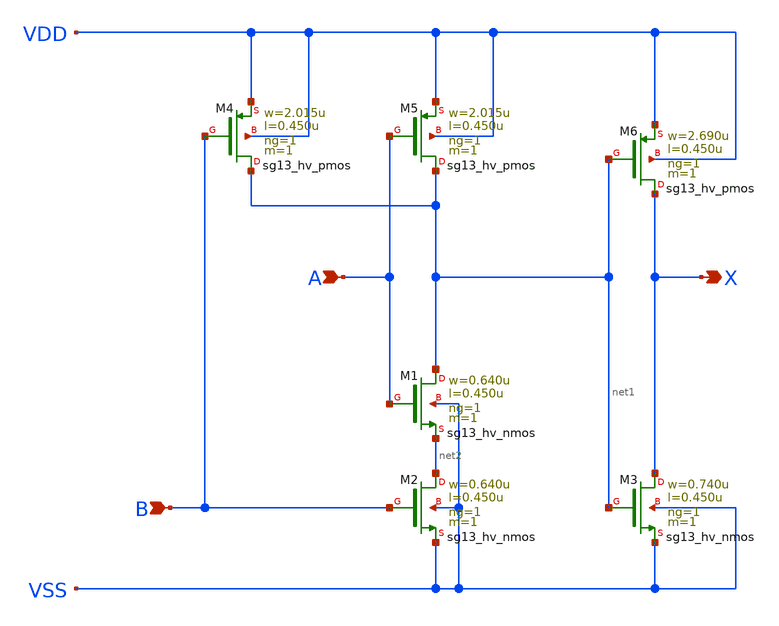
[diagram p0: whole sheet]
** sch_path: ihp-sg13g2/libs.ref/sg13g2_stdcell_hv/sch/xschem/sg13g2_hv_and2_1.sch
* Copyright 2023 IHP PDK Authors
* Licensed under the Apache License, Version 2.0 (the "License");
* you may not use this file except in compliance with the License.
* You may obtain a copy of the License at
* https://www.apache.org/licenses/LICENSE-2.0
* Unless required by applicable law or agreed to in writing, software
* distributed under the License is distributed on an "AS IS" BASIS,
* WITHOUT WARRANTIES OR CONDITIONS OF ANY KIND, either express or implied.
* See the License for the specific language governing permissions and
* limitations under the License.
**.subckt sg13g2_hv_and2_1 A B X
*.ipin A
*.ipin B
*.opin X
XM1 net1 A net2 VSS sg13_hv_nmos w=0.640u l=0.450u ng=1 m=1 mm_ok=1
XM2 net2 B VSS VSS sg13_hv_nmos w=0.640u l=0.450u ng=1 m=1 mm_ok=1
XM3 X net1 VSS VSS sg13_hv_nmos w=0.740u l=0.450u ng=1 m=1 mm_ok=1
XM4 net1 B VDD VDD sg13_hv_pmos w=2.015u l=0.450u ng=1 m=1 mm_ok=1
XM5 net1 A VDD VDD sg13_hv_pmos w=2.015u l=0.450u ng=1 m=1 mm_ok=1
XM6 X net1 VDD VDD sg13_hv_pmos w=2.690u l=0.450u ng=1 m=1 mm_ok=1
**.ends
.end
